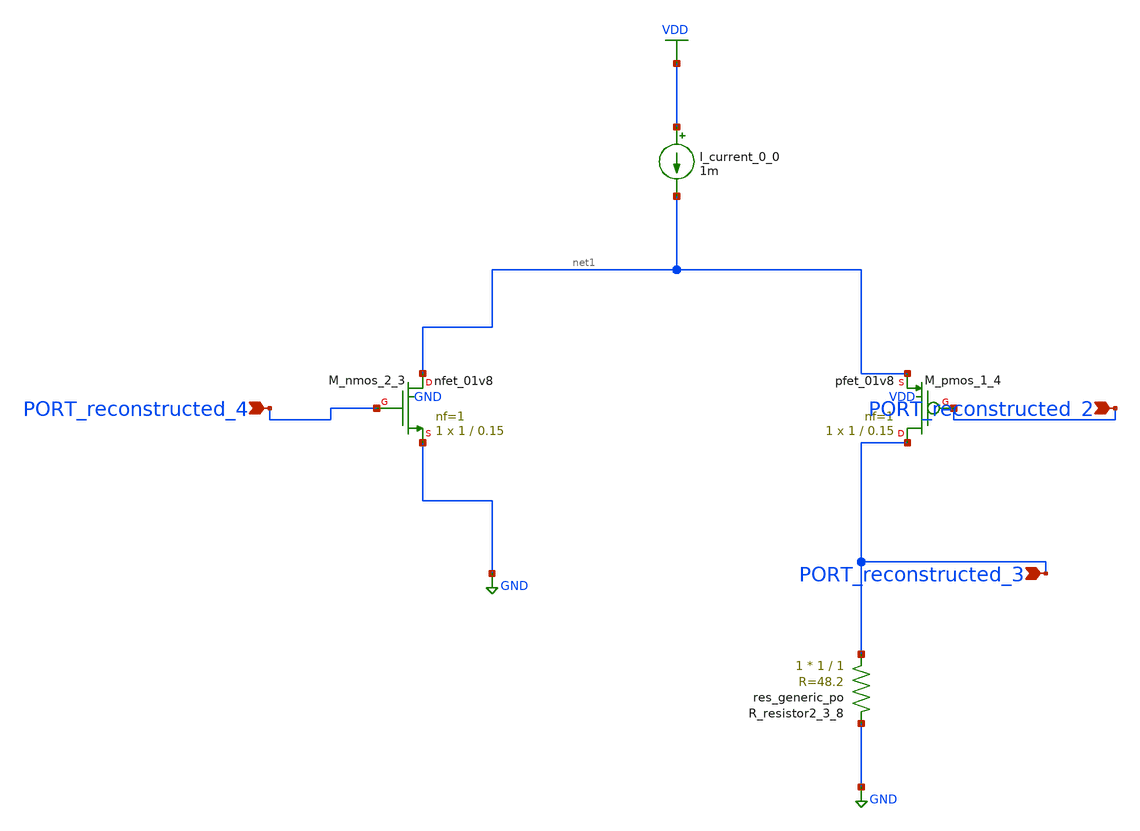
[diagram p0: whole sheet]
** sch_path: schematics/AMSNet/142.sch
**.subckt 142 PORT_reconstructed_2 PORT_reconstructed_3 PORT_reconstructed_4
*.ipin PORT_reconstructed_2
*.ipin PORT_reconstructed_3
*.ipin PORT_reconstructed_4
I_current_0_0 VDD net1 1m
XM_nmos_2_3 net1 PORT_reconstructed_4 GND GND sky130_fd_pr__nfet_01v8 L=0.15 W=1 nf=1 ad='int((1 + 1)/2) * 1 / 1 * 0.29'
+ as='int((1 + 2)/2) * 1 / 1 * 0.29' pd='2*int((1 + 1)/2) * (1 / 1 + 0.29)' ps='2*int((1 + 2)/2) * (1 / 1 + 0.29)'
+ nrd='0.29 / 1 ' nrs='0.29 / 1 ' sa=0 sb=0 sd=0 mult=1 m=1
XM_pmos_1_4 PORT_reconstructed_3 PORT_reconstructed_2 net1 VDD sky130_fd_pr__pfet_01v8 L=0.15 W=1 nf=1
+ ad='int((1 + 1)/2) * 1 / 1 * 0.29' as='int((1 + 2)/2) * 1 / 1 * 0.29' pd='2*int((1 + 1)/2) * (1 / 1 + 0.29)'
+ ps='2*int((1 + 2)/2) * (1 / 1 + 0.29)' nrd='0.29 / 1 ' nrs='0.29 / 1 ' sa=0 sb=0 sd=0 mult=1 m=1
XR_resistor2_3_8 PORT_reconstructed_3 GND sky130_fd_pr__res_generic_po W=1 L=1 m=1
**.ends
.GLOBAL GND
.GLOBAL VDD
.end
